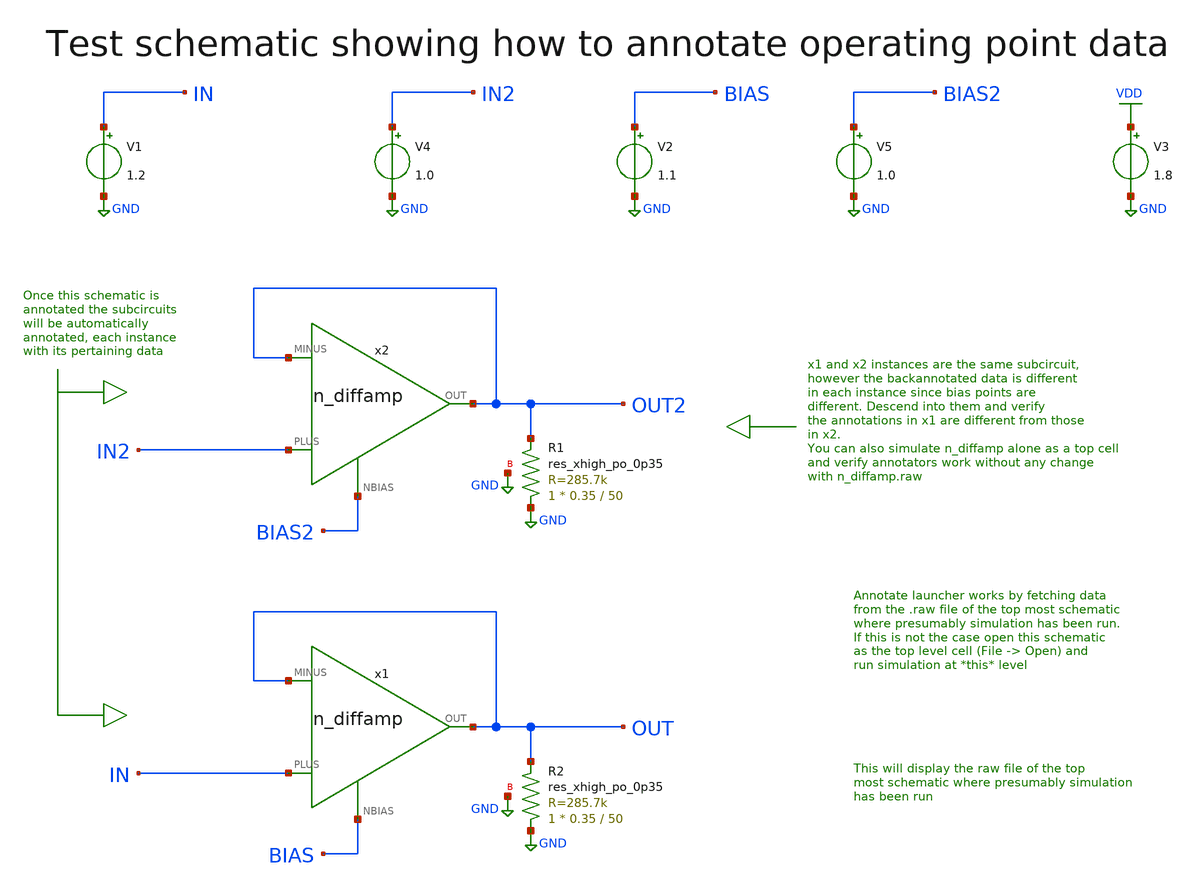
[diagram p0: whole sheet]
** sch_path: sky130A/xschem_libs/sky130_tests_ase/test_analog/schematic/test_analog.sch
* Copyright 2021 Stefan Frederik Schippers
* Licensed under the Apache License, Version 2.0 (the "License");
* you may not use this file except in compliance with the License.
* You may obtain a copy of the License at
* https://www.apache.org/licenses/LICENSE-2.0
* Unless required by applicable law or agreed to in writing, software
* distributed under the License is distributed on an "AS IS" BASIS,
* WITHOUT WARRANTIES OR CONDITIONS OF ANY KIND, either express or implied.
* See the License for the specific language governing permissions and
* limitations under the License.
**.subckt test_analog
x1 OUT OUT IN BIAS n_diffamp
x2 OUT2 OUT2 IN2 BIAS2 n_diffamp
V1 IN GND 1.2
V2 BIAS GND 1.1
V3 VDD GND 1.8
V4 IN2 GND 1.0
V5 BIAS2 GND 1.0
XR1 GND OUT2 GND sky130_fd_pr__res_xhigh_po_0p35 L=50 mult=1 m=1
XR2 GND OUT GND sky130_fd_pr__res_xhigh_po_0p35 L=50 mult=1 m=1
**.ends
.GLOBAL GND
.GLOBAL VDD
.end
